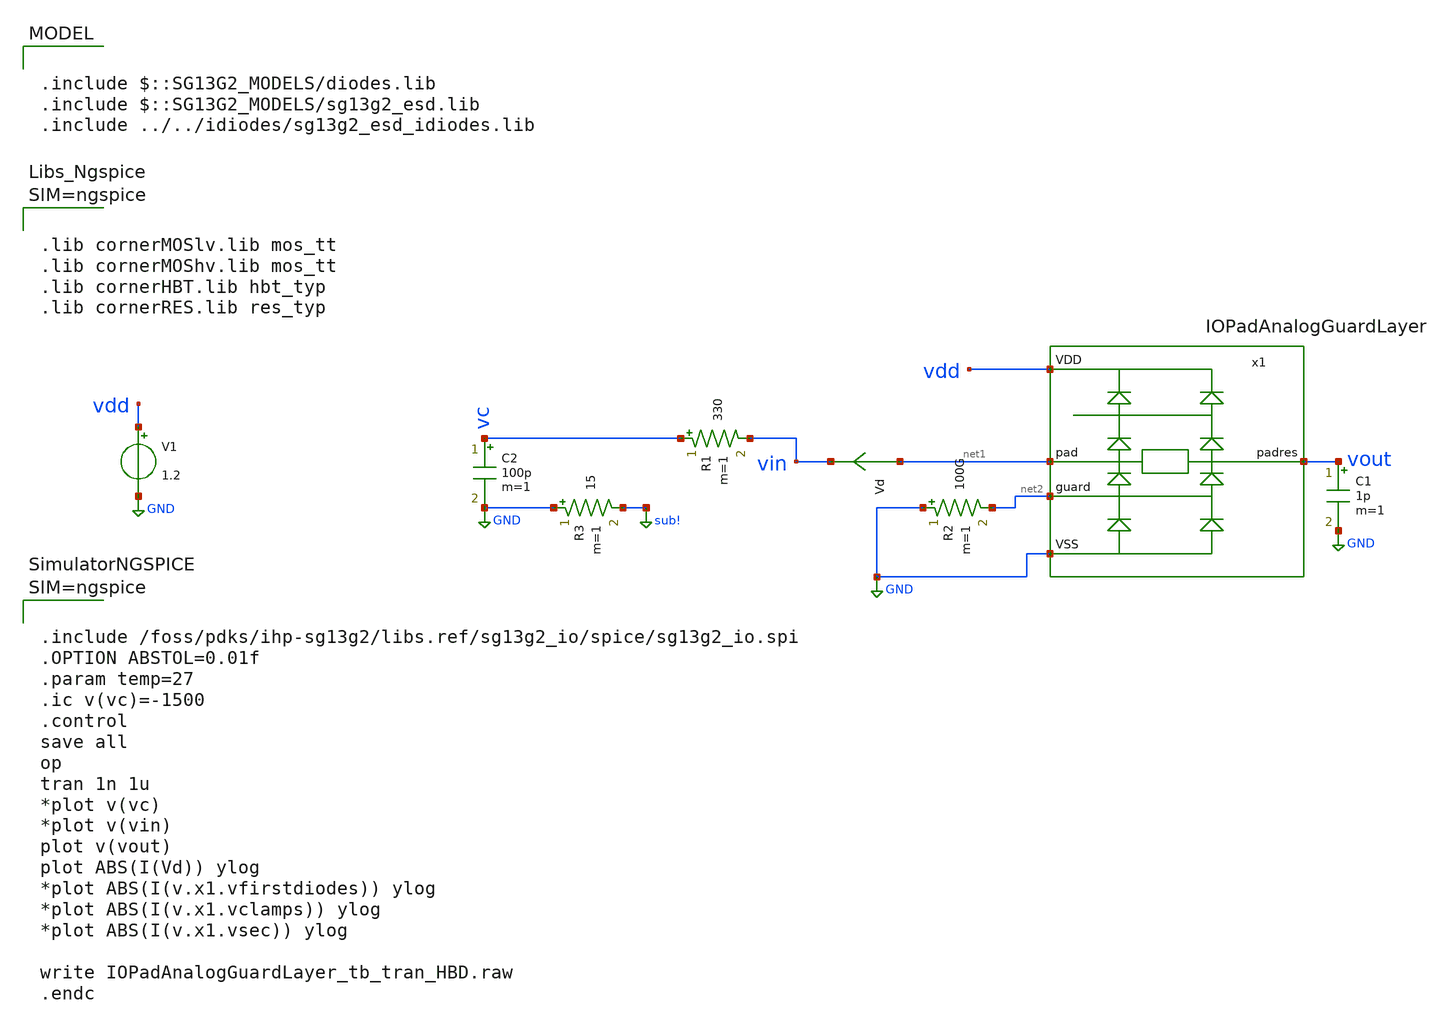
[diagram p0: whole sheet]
** sch_path: trident_test_structures/design_data/xschem/IOPadAnalogGuardLayer/IOPadAnalogGuardLayer_tb_tran_HBD.sch
**.subckt IOPadAnalogGuardLayer_tb_tran_HBD
V1 vdd GND 1.2
Vd net1 vin 0
.save i(vd)
C1 vout GND 1p m=1
C2 vc GND 100p m=1
R1 vc vin 330 m=1
R2 GND net2 100G m=1
R3 GND sub! 15 m=1
x1 vdd net1 vout net2 GND IOPadAnalogGuardLayer
**** begin user architecture code



.lib cornerMOSlv.lib mos_tt
.lib cornerMOShv.lib mos_tt
.lib cornerHBT.lib hbt_typ
.lib cornerRES.lib res_typ






.include /foss/pdks/ihp-sg13g2/libs.ref/sg13g2_io/spice/sg13g2_io.spi
.OPTION ABSTOL=0.01f
.param temp=27
.ic v(vc)=-1500
.control
save all
op
tran 1n 1u
*plot v(vc)
*plot v(vin)
plot v(vout)
plot ABS(I(Vd)) ylog
*plot ABS(I(v.x1.vfirstdiodes)) ylog
*plot ABS(I(v.x1.vclamps)) ylog
*plot ABS(I(v.x1.vsec)) ylog

write IOPadAnalogGuardLayer_tb_tran_HBD.raw
.endc




.include $::SG13G2_MODELS/diodes.lib
.include $::SG13G2_MODELS/sg13g2_esd.lib
.include ../../idiodes/sg13g2_esd_idiodes.lib

**** end user architecture code
**.ends
.GLOBAL GND
.GLOBAL sub!
.end
